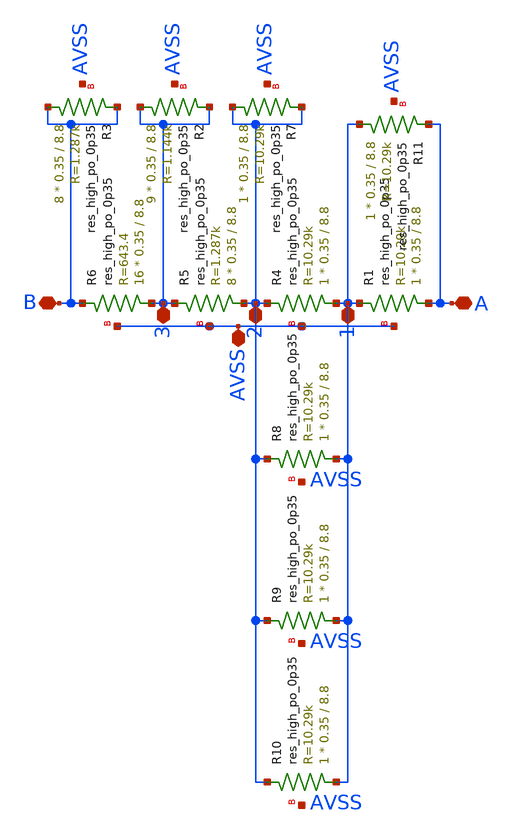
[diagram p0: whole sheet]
** sch_path: magic/res_trim.sch
**.subckt res_trim B A AVSS 1 2 3
*.iopin B
*.iopin A
*.iopin AVSS
*.iopin 1
*.iopin 2
*.iopin 3
XR1 A 1 AVSS sky130_fd_pr__res_high_po_0p35 L=8.8 mult=1 m=1
XR4 1 2 AVSS sky130_fd_pr__res_high_po_0p35 L=8.8 mult=1 m=1
XR5 2 3 AVSS sky130_fd_pr__res_high_po_0p35 L=8.8 mult=8 m=8
XR6 3 B AVSS sky130_fd_pr__res_high_po_0p35 L=8.8 mult=16 m=16
XR2 3 3 AVSS sky130_fd_pr__res_high_po_0p35 L=8.8 mult=9 m=9
XR3 B B AVSS sky130_fd_pr__res_high_po_0p35 L=8.8 mult=8 m=8
XR7 2 2 AVSS sky130_fd_pr__res_high_po_0p35 L=8.8 mult=1 m=1
XR8 1 2 AVSS sky130_fd_pr__res_high_po_0p35 L=8.8 mult=1 m=1
XR9 1 2 AVSS sky130_fd_pr__res_high_po_0p35 L=8.8 mult=1 m=1
XR10 1 2 AVSS sky130_fd_pr__res_high_po_0p35 L=8.8 mult=1 m=1
XR11 1 A AVSS sky130_fd_pr__res_high_po_0p35 L=8.8 mult=1 m=1
**.ends
.end
